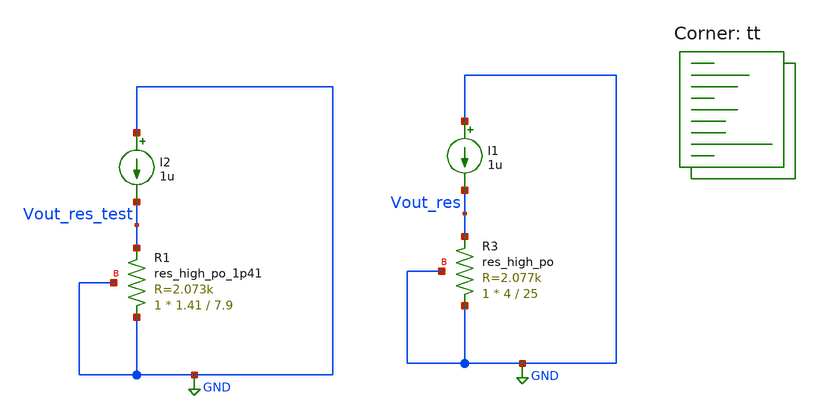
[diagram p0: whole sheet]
** sch_path: xschem/misc/testing/res.sch
**.subckt res
I1 GND Vout_res 1u
XR3 GND Vout_res GND sky130_fd_pr__res_high_po W=4 L=25 mult=1 m=1
I2 GND Vout_res_test 1u
XR1 GND Vout_res_test GND sky130_fd_pr__res_high_po_1p41 L=7.9 mult=1 m=1
**** begin user architecture code
.lib $::SKYWATER_MODELS/sky130.lib.spice tt


.param temp=27

.dc temp -40 125 1


.save all
.control
run
plot Vout_res Vout_res_test
plot deriv(Vout_res) deriv(Vout_res_test)
.endc



**** end user architecture code
**.ends
.GLOBAL GND
.end
